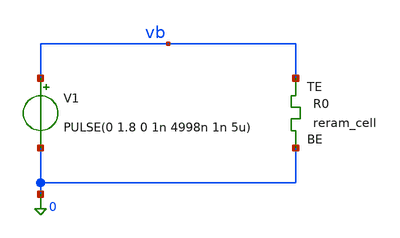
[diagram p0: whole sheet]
** sch_path: memristor_models/sky130_original/1R_saw.sch
**.subckt 1R_saw
V1 vb 0 PULSE(0 1.8 0 1n 4998n 1n 5u)
XR0 vb 0 sky130_fd_pr_reram__reram_cell Tfilament_0=3.3e-9
**** begin user architecture code

** opencircuitdesign pdks install
.inc $::SKYWATER_MODELS/sky130_fd_pr_reram__reram_cell.spice



.tran 50n 2000u
.control
	savecurrents
	save all
	run
	write 1R_saw.raw
.endc



**** end user architecture code
**.ends
.end
